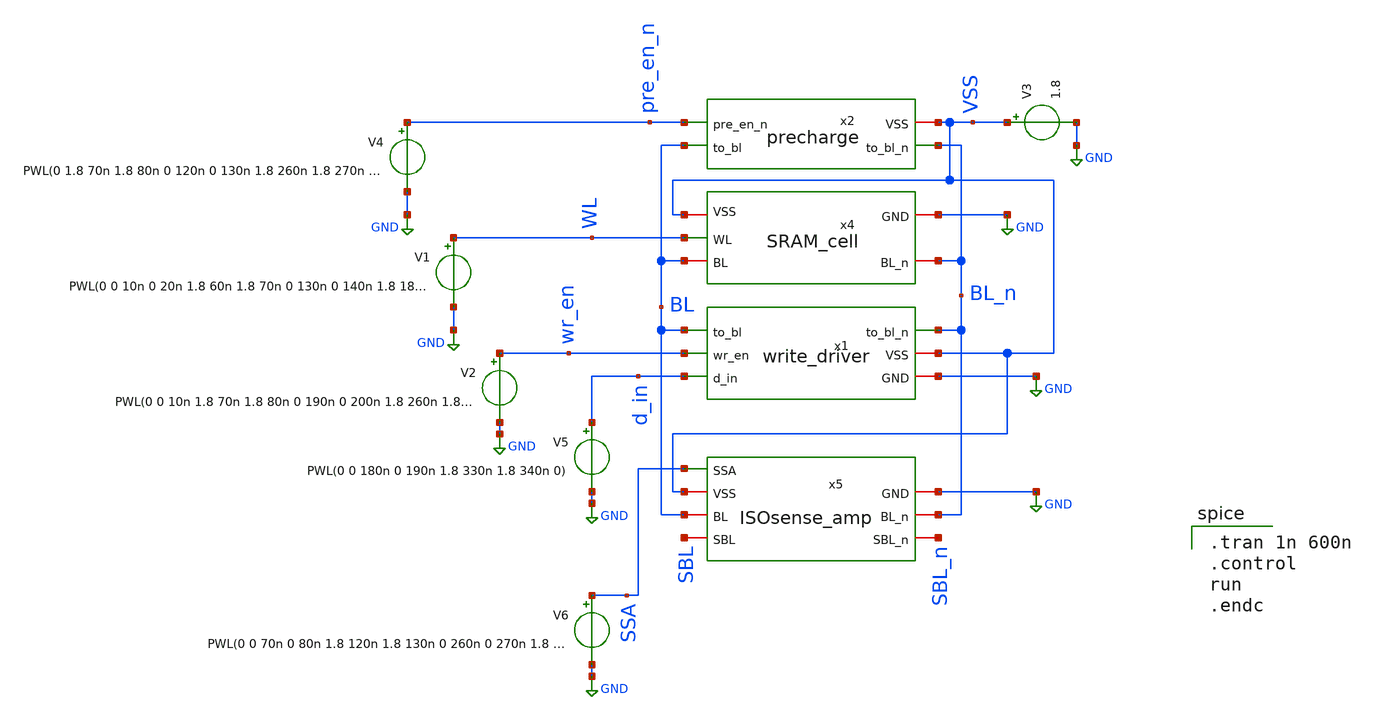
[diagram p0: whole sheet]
** sch_path: sense_amp_full.sch
**.subckt sense_amp_full
V3 VSS GND 1.8
V1 WL GND PWL(0 0 10n 0 20n 1.8 60n 1.8 70n 0 130n 0 140n 1.8 180n 1.8 190n 0 200n 0 210n 1.8 250n
+ 1.8 260n 0 320n 0 330n 1.8 370n 1.8 380n 0 390n 0 400n 1.8 440n 1.8 450n 0 510n 0 520n 1.8)
V2 wr_en GND PWL(0 0 10n 1.8 70n 1.8 80n 0 190n 0 200n 1.8 260n 1.8 270n 0 380n 0 390n 1.8 450n 1.8
+ 460n 0)
V4 pre_en_n GND PWL(0 1.8 70n 1.8 80n 0 120n 0 130n 1.8 260n 1.8 270n 0 310n 0 320n 1.8 450n 1.8
+ 460n 0 500n 0 510n 1.8)
V5 d_in GND PWL(0 0 180n 0 190n 1.8 330n 1.8 340n 0)
x2 VSS BL_n BL pre_en_n precharge
x4 WL VSS BL_n BL GND SRAM_cell
x1 BL_n BL wr_en VSS d_in GND write_driver
V6 SSA GND PWL(0 0 70n 0 80n 1.8 120n 1.8 130n 0 260n 0 270n 1.8 310n 1.8 320n 0 450n 0 460n 1.8
+ 500n 1.8 510n 0)
x5 SSA BL BL_n VSS SBL SBL_n GND ISOsense_amp
**** begin user architecture code
 .lib $::SKYWATER_MODELS/sky130.lib.spice tt

.tran 1n 600n
.control
run
.endc

**** end user architecture code
**.ends

* expanding   symbol:  EE431_FINALPROJECT/proj_SRAM/precharge.sym # of pins=4
** sym_path: precharge.sym
** sch_path: precharge.sch
.subckt precharge VSS to_bl_n to_bl pre_en_n
*.ipin pre_en_n
*.opin to_bl
*.opin to_bl_n
*.iopin VSS
XM1 to_bl_n pre_en_n VSS VSS sky130_fd_pr__pfet_01v8 L=0.25 W=0.5 nf=1 ad='int((nf+1)/2) * W/nf * 0.29'
+ as='int((nf+2)/2) * W/nf * 0.29' pd='2*int((nf+1)/2) * (W/nf + 0.29)' ps='2*int((nf+2)/2) * (W/nf + 0.29)'
+ nrd='0.29 / W' nrs='0.29 / W' sa=0 sb=0 sd=0 mult=1 m=1
XM2 to_bl pre_en_n VSS VSS sky130_fd_pr__pfet_01v8 L=0.25 W=0.5 nf=1 ad='int((nf+1)/2) * W/nf * 0.29'
+ as='int((nf+2)/2) * W/nf * 0.29' pd='2*int((nf+1)/2) * (W/nf + 0.29)' ps='2*int((nf+2)/2) * (W/nf + 0.29)'
+ nrd='0.29 / W' nrs='0.29 / W' sa=0 sb=0 sd=0 mult=1 m=1
.ends


* expanding   symbol:  EE431_FINALPROJECT/proj_SRAM/SRAM_cell.sym # of pins=5
** sym_path: SRAM_cell.sym
** sch_path: SRAM_cell.sch
.subckt SRAM_cell WL VSS BL_n BL GND
*.ipin WL
*.iopin BL
*.iopin BL_n
*.iopin VSS
*.iopin GND
XM1 Q_n Q GND GND sky130_fd_pr__nfet_01v8 L=0.25 W=1.25 nf=1 ad='int((nf+1)/2) * W/nf * 0.29' as='int((nf+2)/2) * W/nf * 0.29'
+ pd='2*int((nf+1)/2) * (W/nf + 0.29)' ps='2*int((nf+2)/2) * (W/nf + 0.29)' nrd='0.29 / W' nrs='0.29 / W'
+ sa=0 sb=0 sd=0 mult=1 m=1
XM2 Q_n Q VSS VSS sky130_fd_pr__pfet_01v8 L=0.25 W=0.5 nf=1 ad='int((nf+1)/2) * W/nf * 0.29' as='int((nf+2)/2) * W/nf * 0.29'
+ pd='2*int((nf+1)/2) * (W/nf + 0.29)' ps='2*int((nf+2)/2) * (W/nf + 0.29)' nrd='0.29 / W' nrs='0.29 / W'
+ sa=0 sb=0 sd=0 mult=1 m=1
XM3 Q Q_n GND GND sky130_fd_pr__nfet_01v8 L=0.25 W=1.25 nf=1 ad='int((nf+1)/2) * W/nf * 0.29' as='int((nf+2)/2) * W/nf * 0.29'
+ pd='2*int((nf+1)/2) * (W/nf + 0.29)' ps='2*int((nf+2)/2) * (W/nf + 0.29)' nrd='0.29 / W' nrs='0.29 / W'
+ sa=0 sb=0 sd=0 mult=1 m=1
XM4 Q Q_n VSS VSS sky130_fd_pr__pfet_01v8 L=0.25 W=0.5 nf=1 ad='int((nf+1)/2) * W/nf * 0.29' as='int((nf+2)/2) * W/nf * 0.29'
+ pd='2*int((nf+1)/2) * (W/nf + 0.29)' ps='2*int((nf+2)/2) * (W/nf + 0.29)' nrd='0.29 / W' nrs='0.29 / W'
+ sa=0 sb=0 sd=0 mult=1 m=1
XM5 Q WL BL GND sky130_fd_pr__nfet_01v8 L=0.25 W=0.75 nf=1 ad='int((nf+1)/2) * W/nf * 0.29' as='int((nf+2)/2) * W/nf * 0.29'
+ pd='2*int((nf+1)/2) * (W/nf + 0.29)' ps='2*int((nf+2)/2) * (W/nf + 0.29)' nrd='0.29 / W' nrs='0.29 / W'
+ sa=0 sb=0 sd=0 mult=1 m=1
XM6 Q_n WL BL_n GND sky130_fd_pr__nfet_01v8 L=0.25 W=0.75 nf=1 ad='int((nf+1)/2) * W/nf * 0.29' as='int((nf+2)/2) * W/nf * 0.29'
+ pd='2*int((nf+1)/2) * (W/nf + 0.29)' ps='2*int((nf+2)/2) * (W/nf + 0.29)' nrd='0.29 / W' nrs='0.29 / W'
+ sa=0 sb=0 sd=0 mult=1 m=1
.ends


* expanding   symbol:  EE431_FINALPROJECT/proj_SRAM/write_driver.sym # of pins=6
** sym_path: write_driver.sym
** sch_path: write_driver.sch
.subckt write_driver to_bl_n to_bl wr_en VSS d_in GND
*.ipin d_in
*.ipin wr_en
*.opin to_bl
*.opin to_bl_n
*.iopin VSS
*.iopin GND
XM1 to_bl wr_en d_in GND sky130_fd_pr__nfet_01v8 L=0.25 W=1 nf=1 ad='int((nf+1)/2) * W/nf * 0.29' as='int((nf+2)/2) * W/nf * 0.29'
+ pd='2*int((nf+1)/2) * (W/nf + 0.29)' ps='2*int((nf+2)/2) * (W/nf + 0.29)' nrd='0.29 / W' nrs='0.29 / W'
+ sa=0 sb=0 sd=0 mult=1 m=1
XM2 to_bl_n wr_en d_n GND sky130_fd_pr__nfet_01v8 L=0.25 W=1 nf=1 ad='int((nf+1)/2) * W/nf * 0.29' as='int((nf+2)/2) * W/nf * 0.29'
+ pd='2*int((nf+1)/2) * (W/nf + 0.29)' ps='2*int((nf+2)/2) * (W/nf + 0.29)' nrd='0.29 / W' nrs='0.29 / W'
+ sa=0 sb=0 sd=0 mult=1 m=1
XM3 d_n d_in VSS VSS sky130_fd_pr__pfet_01v8 L=0.25 W=1 nf=1 ad='int((nf+1)/2) * W/nf * 0.29' as='int((nf+2)/2) * W/nf * 0.29'
+ pd='2*int((nf+1)/2) * (W/nf + 0.29)' ps='2*int((nf+2)/2) * (W/nf + 0.29)' nrd='0.29 / W' nrs='0.29 / W'
+ sa=0 sb=0 sd=0 mult=1 m=1
XM4 d_n d_in GND GND sky130_fd_pr__nfet_01v8 L=0.25 W=0.5 nf=1 ad='int((nf+1)/2) * W/nf * 0.29' as='int((nf+2)/2) * W/nf * 0.29'
+ pd='2*int((nf+1)/2) * (W/nf + 0.29)' ps='2*int((nf+2)/2) * (W/nf + 0.29)' nrd='0.29 / W' nrs='0.29 / W'
+ sa=0 sb=0 sd=0 mult=1 m=1
.ends


* expanding   symbol:  EE431_FINALPROJECT/proj_SRAM/ISOsense_amp.sym # of pins=7
** sym_path: ISOsense_amp.sym
** sch_path: ISOsense_amp.sch
.subckt ISOsense_amp SSA BL BL_n VSS SBL SBL_n GND
*.iopin VSS
*.iopin BL_n
*.iopin BL
*.iopin GND
*.ipin SSA
*.iopin SBL
*.iopin SBL_n
XM1 SBL_n SBL net1 GND sky130_fd_pr__nfet_01v8 L=0.25 W=1 nf=1 ad='int((nf+1)/2) * W/nf * 0.29' as='int((nf+2)/2) * W/nf * 0.29'
+ pd='2*int((nf+1)/2) * (W/nf + 0.29)' ps='2*int((nf+2)/2) * (W/nf + 0.29)' nrd='0.29 / W' nrs='0.29 / W'
+ sa=0 sb=0 sd=0 mult=1 m=1
XM2 SBL SBL_n net1 GND sky130_fd_pr__nfet_01v8 L=0.25 W=1 nf=1 ad='int((nf+1)/2) * W/nf * 0.29' as='int((nf+2)/2) * W/nf * 0.29'
+ pd='2*int((nf+1)/2) * (W/nf + 0.29)' ps='2*int((nf+2)/2) * (W/nf + 0.29)' nrd='0.29 / W' nrs='0.29 / W'
+ sa=0 sb=0 sd=0 mult=1 m=1
XM3 SBL_n SBL VSS VSS sky130_fd_pr__pfet_01v8 L=0.25 W=2 nf=1 ad='int((nf+1)/2) * W/nf * 0.29' as='int((nf+2)/2) * W/nf * 0.29'
+ pd='2*int((nf+1)/2) * (W/nf + 0.29)' ps='2*int((nf+2)/2) * (W/nf + 0.29)' nrd='0.29 / W' nrs='0.29 / W'
+ sa=0 sb=0 sd=0 mult=1 m=1
XM4 SBL SBL_n VSS VSS sky130_fd_pr__pfet_01v8 L=0.25 W=2 nf=1 ad='int((nf+1)/2) * W/nf * 0.29' as='int((nf+2)/2) * W/nf * 0.29'
+ pd='2*int((nf+1)/2) * (W/nf + 0.29)' ps='2*int((nf+2)/2) * (W/nf + 0.29)' nrd='0.29 / W' nrs='0.29 / W'
+ sa=0 sb=0 sd=0 mult=1 m=1
XM5 net1 SSA GND GND sky130_fd_pr__nfet_01v8 L=0.25 W=2 nf=1 ad='int((nf+1)/2) * W/nf * 0.29' as='int((nf+2)/2) * W/nf * 0.29'
+ pd='2*int((nf+1)/2) * (W/nf + 0.29)' ps='2*int((nf+2)/2) * (W/nf + 0.29)' nrd='0.29 / W' nrs='0.29 / W'
+ sa=0 sb=0 sd=0 mult=1 m=1
XM6 SBL SSA BL VSS sky130_fd_pr__pfet_01v8 L=0.25 W=0.5 nf=1 ad='int((nf+1)/2) * W/nf * 0.29' as='int((nf+2)/2) * W/nf * 0.29'
+ pd='2*int((nf+1)/2) * (W/nf + 0.29)' ps='2*int((nf+2)/2) * (W/nf + 0.29)' nrd='0.29 / W' nrs='0.29 / W'
+ sa=0 sb=0 sd=0 mult=1 m=1
XM7 SBL_n SSA BL_n VSS sky130_fd_pr__pfet_01v8 L=0.25 W=0.5 nf=1 ad='int((nf+1)/2) * W/nf * 0.29' as='int((nf+2)/2) * W/nf * 0.29'
+ pd='2*int((nf+1)/2) * (W/nf + 0.29)' ps='2*int((nf+2)/2) * (W/nf + 0.29)' nrd='0.29 / W' nrs='0.29 / W'
+ sa=0 sb=0 sd=0 mult=1 m=1
.ends

.GLOBAL GND
.end
